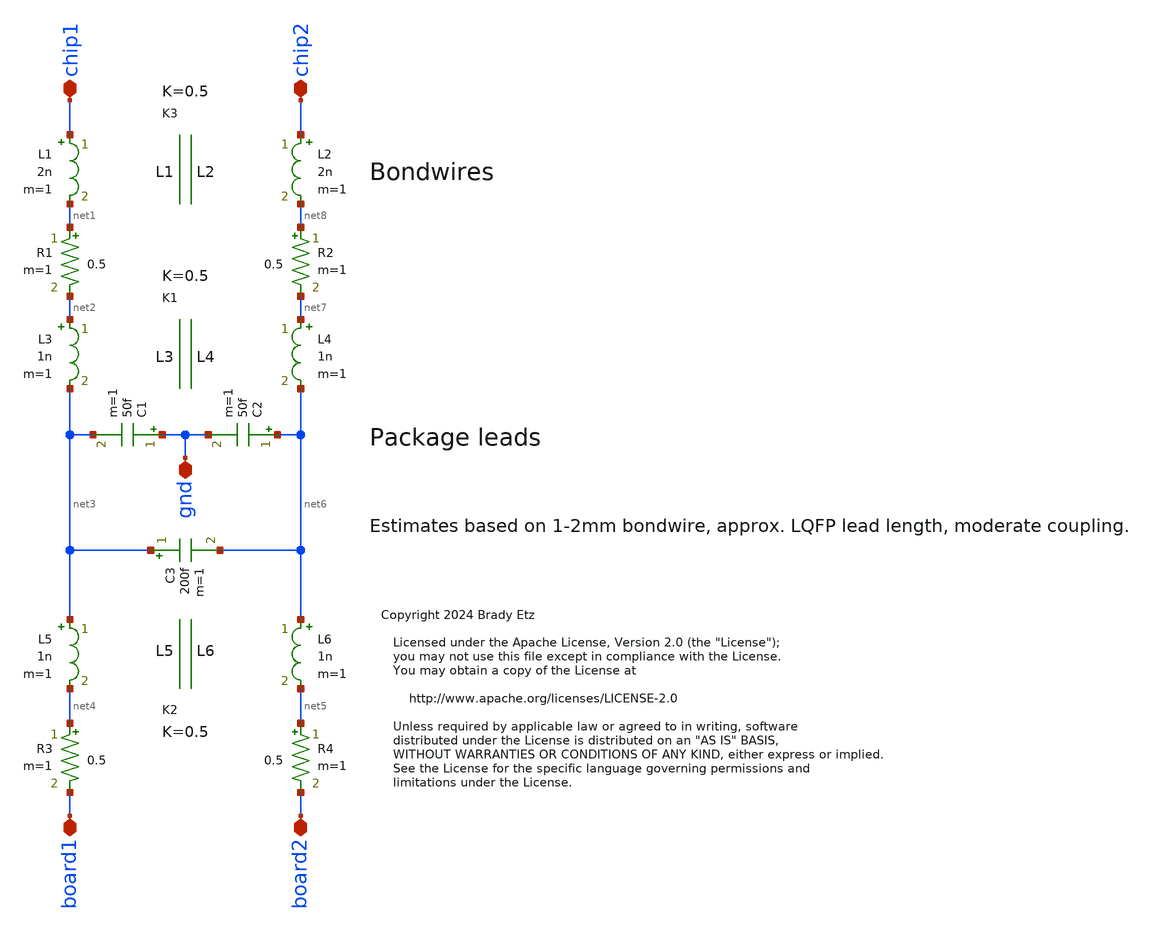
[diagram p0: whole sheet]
** sch_path: xschem/lqfp_parasitics.sch
* Copyright 2024 Brady Etz
* Licensed under the Apache License, Version 2.0 (the "License");
**.subckt lqfp_parasitics chip1 chip2 board2 board1 gnd
*.iopin chip1
*.iopin chip2
*.iopin board2
*.iopin board1
*.iopin gnd
L5 net3 net4 1n m=1
L6 net6 net5 1n m=1
K1 L3 L4 0.5
L3 net2 net3 1n m=1
L4 net7 net6 1n m=1
C3 net3 net6 200f m=1
C2 net6 gnd 50f m=1
C1 gnd net3 50f m=1
R4 net5 board2 0.5 m=1
R3 net4 board1 0.5 m=1
K2 L5 L6 0.5
R2 net8 net7 0.5 m=1
R1 net1 net2 0.5 m=1
L1 chip1 net1 2n m=1
L2 chip2 net8 2n m=1
K3 L1 L2 0.5
**.ends
.end
